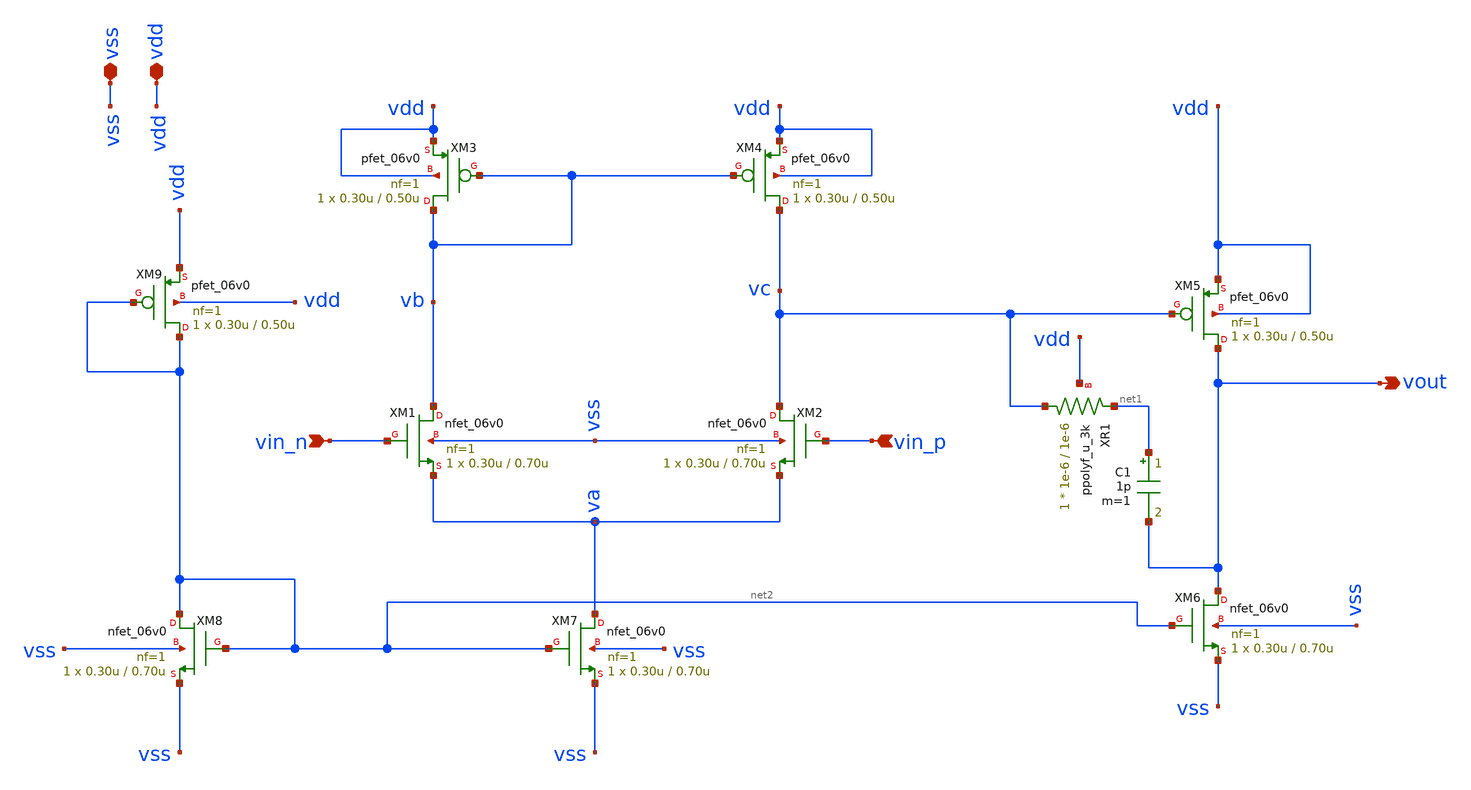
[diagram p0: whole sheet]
** sch_path: analog-db/circuits/ldo_005_buffered_ref/reference/ti-ldo/ref_amp/ref_amp_real_current_source.sch
**.subckt ref_amp_real_current_source vin_n vin_p vdd vss vout
*.ipin vin_n
*.ipin vin_p
*.iopin vdd
*.iopin vss
*.opin vout
XM1 vb vin_n va vss nfet_06v0 L=0.70u W=0.30u nf=1 ad='int((nf+1)/2) * W/nf * 0.18u' as='int((nf+2)/2) * W/nf * 0.18u'
+ pd='2*int((nf+1)/2) * (W/nf + 0.18u)' ps='2*int((nf+2)/2) * (W/nf + 0.18u)' nrd='0.18u / W' nrs='0.18u / W'
+ sa=0 sb=0 sd=0 m=1
XM2 vc vin_p va vss nfet_06v0 L=0.70u W=0.30u nf=1 ad='int((nf+1)/2) * W/nf * 0.18u' as='int((nf+2)/2) * W/nf * 0.18u'
+ pd='2*int((nf+1)/2) * (W/nf + 0.18u)' ps='2*int((nf+2)/2) * (W/nf + 0.18u)' nrd='0.18u / W' nrs='0.18u / W'
+ sa=0 sb=0 sd=0 m=1
XM3 vb vb vdd vdd pfet_06v0 L=0.50u W=0.30u nf=1 ad='int((nf+1)/2) * W/nf * 0.18u' as='int((nf+2)/2) * W/nf * 0.18u'
+ pd='2*int((nf+1)/2) * (W/nf + 0.18u)' ps='2*int((nf+2)/2) * (W/nf + 0.18u)' nrd='0.18u / W' nrs='0.18u / W'
+ sa=0 sb=0 sd=0 m=1
XM4 vc vb vdd vdd pfet_06v0 L=0.50u W=0.30u nf=1 ad='int((nf+1)/2) * W/nf * 0.18u' as='int((nf+2)/2) * W/nf * 0.18u'
+ pd='2*int((nf+1)/2) * (W/nf + 0.18u)' ps='2*int((nf+2)/2) * (W/nf + 0.18u)' nrd='0.18u / W' nrs='0.18u / W'
+ sa=0 sb=0 sd=0 m=1
XM5 vout vc vdd vdd pfet_06v0 L=0.50u W=0.30u nf=1 ad='int((nf+1)/2) * W/nf * 0.18u' as='int((nf+2)/2) * W/nf * 0.18u'
+ pd='2*int((nf+1)/2) * (W/nf + 0.18u)' ps='2*int((nf+2)/2) * (W/nf + 0.18u)' nrd='0.18u / W' nrs='0.18u / W'
+ sa=0 sb=0 sd=0 m=1
C1 net1 vout 1p m=1
XR1 vc net1 vdd ppolyf_u_3k r_width=1e-6 r_length=1e-6 m=1
XM6 vout net2 vss vss nfet_06v0 L=0.70u W=0.30u nf=1 ad='int((nf+1)/2) * W/nf * 0.18u' as='int((nf+2)/2) * W/nf * 0.18u'
+ pd='2*int((nf+1)/2) * (W/nf + 0.18u)' ps='2*int((nf+2)/2) * (W/nf + 0.18u)' nrd='0.18u / W' nrs='0.18u / W'
+ sa=0 sb=0 sd=0 m=1
XM7 va net2 vss vss nfet_06v0 L=0.70u W=0.30u nf=1 ad='int((nf+1)/2) * W/nf * 0.18u' as='int((nf+2)/2) * W/nf * 0.18u'
+ pd='2*int((nf+1)/2) * (W/nf + 0.18u)' ps='2*int((nf+2)/2) * (W/nf + 0.18u)' nrd='0.18u / W' nrs='0.18u / W'
+ sa=0 sb=0 sd=0 m=1
XM8 net2 net2 vss vss nfet_06v0 L=0.70u W=0.30u nf=1 ad='int((nf+1)/2) * W/nf * 0.18u' as='int((nf+2)/2) * W/nf * 0.18u'
+ pd='2*int((nf+1)/2) * (W/nf + 0.18u)' ps='2*int((nf+2)/2) * (W/nf + 0.18u)' nrd='0.18u / W' nrs='0.18u / W'
+ sa=0 sb=0 sd=0 m=1
XM9 net2 net2 vdd vdd pfet_06v0 L=0.50u W=0.30u nf=1 ad='int((nf+1)/2) * W/nf * 0.18u' as='int((nf+2)/2) * W/nf * 0.18u'
+ pd='2*int((nf+1)/2) * (W/nf + 0.18u)' ps='2*int((nf+2)/2) * (W/nf + 0.18u)' nrd='0.18u / W' nrs='0.18u / W'
+ sa=0 sb=0 sd=0 m=1
**.ends
.end
